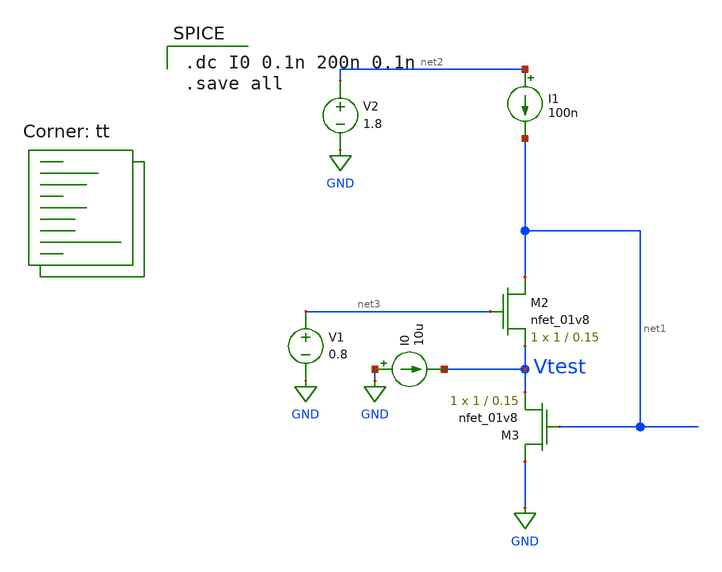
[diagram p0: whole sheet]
** sch_path: test_fvf.sch
**.subckt test_fvf
XM2 net1 net3 Vtest GND sky130_fd_pr__nfet_01v8 L=0.15 W=1 nf=1 ad='int((nf+1)/2) * W/nf * 0.29' as='int((nf+2)/2) * W/nf * 0.29'
+ pd='2*int((nf+1)/2) * (W/nf + 0.29)' ps='2*int((nf+2)/2) * (W/nf + 0.29)' nrd='0.29 / W' nrs='0.29 / W'
+ sa=0 sb=0 sd=0 mult=1 m=1
XM3 GND net1 Vtest GND sky130_fd_pr__nfet_01v8 L=0.15 W=1 nf=1 ad='int((nf+1)/2) * W/nf * 0.29' as='int((nf+2)/2) * W/nf * 0.29'
+ pd='2*int((nf+1)/2) * (W/nf + 0.29)' ps='2*int((nf+2)/2) * (W/nf + 0.29)' nrd='0.29 / W' nrs='0.29 / W'
+ sa=0 sb=0 sd=0 mult=1 m=1
V2 net2 GND 1.8
I0 GND Vtest 10u
I1 net2 net1 100n
V1 net3 GND 0.8
**** begin user architecture code

.dc I0 0.1n 200n 0.1n
.save all

.lib $::SKYWATER_MODELS/sky130.lib.spice tt
**** end user architecture code
**.ends
.GLOBAL GND
.end
